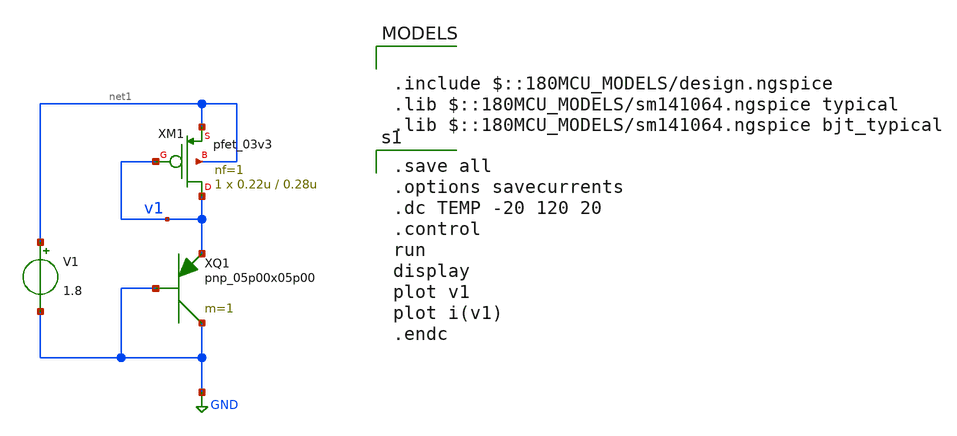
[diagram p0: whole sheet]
** sch_path: GF180/xschem/cmos_vref/Y.Ji_JSSC2019/s1_ctat.sch
**.subckt s1_ctat
XQ1 GND GND v1 pnp_05p00x05p00 m=1
V1 net1 GND 1.8
XM1 v1 v1 net1 net1 pfet_03v3 L=0.28u W=0.22u nf=1 ad='int((nf+1)/2) * W/nf * 0.18u' as='int((nf+2)/2) * W/nf * 0.18u'
+ pd='2*int((nf+1)/2) * (W/nf + 0.18u)' ps='2*int((nf+2)/2) * (W/nf + 0.18u)' nrd='0.18u / W' nrs='0.18u / W'
+ sa=0 sb=0 sd=0 m=1
**** begin user architecture code

.include $::180MCU_MODELS/design.ngspice
.lib $::180MCU_MODELS/sm141064.ngspice typical
.lib $::180MCU_MODELS/sm141064.ngspice bjt_typical


.save all
.options savecurrents
.dc TEMP -20 120 20
.control
run
display
plot v1
plot i(v1)
.endc


**** end user architecture code
**.ends
.GLOBAL GND
.end
